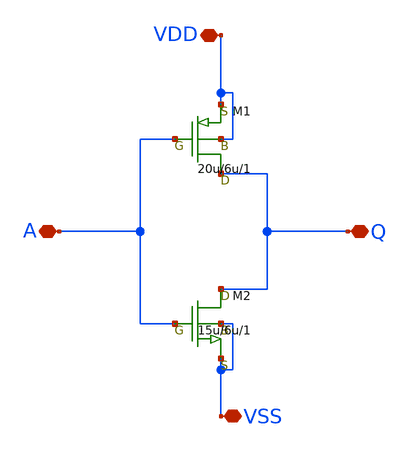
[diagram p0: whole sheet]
** sch_path: samples/inverter/MF20/inverter.sch
**.subckt inverter VDD VSS Q A
*.iopin VDD
*.iopin VSS
*.iopin Q
*.iopin A
M1 Q A VDD VDD pch w=20u l=6u as=0 ps=0 ad=0 pd=0 m=1
M2 Q A VSS VSS nch w=15u l=6u as=0 ps=0 ad=0 pd=0 m=1
**.ends
.end
